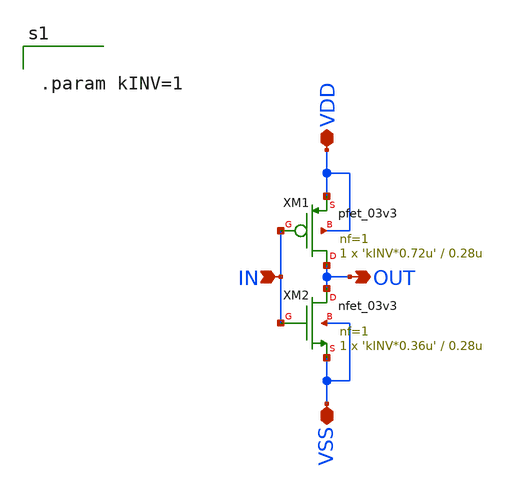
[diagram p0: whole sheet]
** sch_path: CAD6/pc_inv.sch
**.subckt pc_inv IN OUT VDD VSS
*.ipin IN
*.opin OUT
*.iopin VDD
*.iopin VSS
XM1 OUT IN VDD VDD pfet_03v3 L=0.28u W='kINV*0.72u' nf=1 ad='int((nf+1)/2) * W/nf * 0.18u' as='int((nf+2)/2) * W/nf * 0.18u'
+ pd='2*int((nf+1)/2) * (W/nf + 0.18u)' ps='2*int((nf+2)/2) * (W/nf + 0.18u)' nrd='0.18u / W' nrs='0.18u / W'
+ sa=0 sb=0 sd=0 m=1
XM2 OUT IN VSS VSS nfet_03v3 L=0.28u W='kINV*0.36u' nf=1 ad='int((nf+1)/2) * W/nf * 0.18u' as='int((nf+2)/2) * W/nf * 0.18u'
+ pd='2*int((nf+1)/2) * (W/nf + 0.18u)' ps='2*int((nf+2)/2) * (W/nf + 0.18u)' nrd='0.18u / W' nrs='0.18u / W'
+ sa=0 sb=0 sd=0 m=1
**** begin user architecture code


.param kINV=1


**** end user architecture code
**.ends
.end
